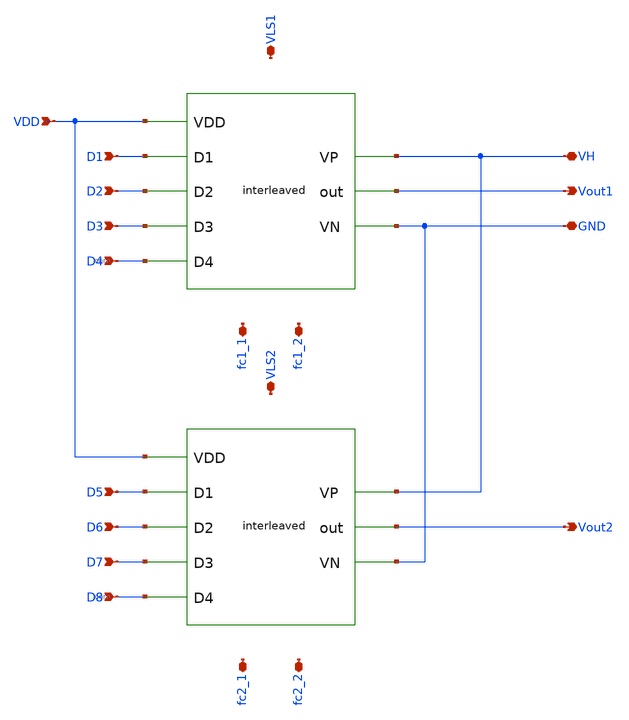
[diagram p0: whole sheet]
** sch_path: xschem/release/interleaved.sch
**.subckt interleaved D1 D2 D3 D4 D5 D6 D7 D8 VH GND Vout1 VDD Vout2 fc1_1 VLS1 VLS2 fc1_2 fc2_1
*+ fc2_2
*.ipin D1
*.ipin D2
*.ipin D3
*.ipin D4
*.ipin D5
*.ipin D6
*.ipin D7
*.ipin D8
*.iopin VH
*.iopin GND
*.opin Vout1
*.ipin VDD
*.opin Vout2
*.iopin fc1_1
*.iopin VLS1
*.iopin VLS2
*.iopin fc1_2
*.iopin fc2_1
*.iopin fc2_2
X1 VDD D6 D5 VH GND Vout2 D7 D8 core
X2 VDD D2 D1 VH GND Vout1 D3 D4 core
**.ends

* expanding   symbol:  core.sym # of pins=8
** sym_path: xschem/release/core.sym
** sch_path: xschem/release/core.sch
.subckt core VDD D2 D1 VP VN out D3 D4
*.opin out
*.iopin VP
*.ipin D1
*.ipin D2
*.ipin D3
*.ipin D4
*.iopin VDD
*.iopin VN
X1 net4 net3 net2 net1 out VP VN VN VN converter
x1 VP net5 net1 VDD level_shifter
x2 VP net6 net2 VDD level_shifter
x3 VP net7 net3 VDD level_shifter
x4 VP net8 net4 VDD level_shifter
.ends


* expanding   symbol:  converter.sym # of pins=9
** sym_path: xschem/hierarchy_sch/converter.sym
** sch_path: xschem/hierarchy_sch/converter.sch
.subckt converter s1 s2 s3 s4 out VP VN fc1_read fc2_read
*.ipin s1
*.ipin s2
*.ipin s3
*.ipin s4
*.iopin VP
*.iopin VN
*.opin fc1_read
*.opin fc2_read
*.iopin out
X1v s1 s2 s3 s4 fc1_read net1 out VP VN power_stage
CFLY fc1_read fc2_read 6.8n m=1
R1 fc2_read net1 0.001 m=1
.ends


* expanding   symbol:  level_shifter.sym # of pins=4
** sym_path: xschem/release/level_shifter.sym
** sch_path: xschem/release/level_shifter.sch
.subckt level_shifter VH vdd OUT IN
*.ipin IN
*.iopin vdd
*.iopin VH
*.opin OUT
XM11 net1 IN vdd vdd sky130_fd_pr__pfet_01v8 L=0.15 W=5 nf=1 ad='int((nf+1)/2) * W/nf * 0.29' as='int((nf+2)/2) * W/nf * 0.29'
+ pd='2*int((nf+1)/2) * (W/nf + 0.29)' ps='2*int((nf+2)/2) * (W/nf + 0.29)' nrd='0.29 / W' nrs='0.29 / W'
+ sa=0 sb=0 sd=0 mult=1 m=1
XM12 net1 IN GND GND sky130_fd_pr__nfet_01v8 L=0.15 W=5 nf=1 ad='int((nf+1)/2) * W/nf * 0.29' as='int((nf+2)/2) * W/nf * 0.29'
+ pd='2*int((nf+1)/2) * (W/nf + 0.29)' ps='2*int((nf+2)/2) * (W/nf + 0.29)' nrd='0.29 / W' nrs='0.29 / W'
+ sa=0 sb=0 sd=0 mult=1 m=1
XM15 net2 net3 VH VH sky130_fd_pr__pfet_g5v0d10v5 L=0.5 W=2 nf=1 ad='int((nf+1)/2) * W/nf * 0.29' as='int((nf+2)/2) * W/nf * 0.29'
+ pd='2*int((nf+1)/2) * (W/nf + 0.29)' ps='2*int((nf+2)/2) * (W/nf + 0.29)' nrd='0.29 / W' nrs='0.29 / W'
+ sa=0 sb=0 sd=0 mult=1 m=1
XM14 net3 net2 VH VH sky130_fd_pr__pfet_g5v0d10v5 L=0.5 W=2 nf=1 ad='int((nf+1)/2) * W/nf * 0.29' as='int((nf+2)/2) * W/nf * 0.29'
+ pd='2*int((nf+1)/2) * (W/nf + 0.29)' ps='2*int((nf+2)/2) * (W/nf + 0.29)' nrd='0.29 / W' nrs='0.29 / W'
+ sa=0 sb=0 sd=0 mult=1 m=1
XM16 net4 net2 VH VH sky130_fd_pr__pfet_g5v0d10v5 L=0.5 W=10 nf=1 ad='int((nf+1)/2) * W/nf * 0.29' as='int((nf+2)/2) * W/nf * 0.29'
+ pd='2*int((nf+1)/2) * (W/nf + 0.29)' ps='2*int((nf+2)/2) * (W/nf + 0.29)' nrd='0.29 / W' nrs='0.29 / W'
+ sa=0 sb=0 sd=0 mult=10 m=10
XM18 net2 net1 GND GND sky130_fd_pr__nfet_g5v0d10v5 L=0.5 W=12 nf=1 ad='int((nf+1)/2) * W/nf * 0.29'
+ as='int((nf+2)/2) * W/nf * 0.29' pd='2*int((nf+1)/2) * (W/nf + 0.29)' ps='2*int((nf+2)/2) * (W/nf + 0.29)'
+ nrd='0.29 / W' nrs='0.29 / W' sa=0 sb=0 sd=0 mult=1 m=1
XM13 net3 IN GND GND sky130_fd_pr__nfet_g5v0d10v5 L=0.5 W=12 nf=1 ad='int((nf+1)/2) * W/nf * 0.29' as='int((nf+2)/2) * W/nf * 0.29'
+ pd='2*int((nf+1)/2) * (W/nf + 0.29)' ps='2*int((nf+2)/2) * (W/nf + 0.29)' nrd='0.29 / W' nrs='0.29 / W'
+ sa=0 sb=0 sd=0 mult=1 m=1
XM17 net4 IN GND GND sky130_fd_pr__nfet_g5v0d10v5 L=0.5 W=10 nf=1 ad='int((nf+1)/2) * W/nf * 0.29' as='int((nf+2)/2) * W/nf * 0.29'
+ pd='2*int((nf+1)/2) * (W/nf + 0.29)' ps='2*int((nf+2)/2) * (W/nf + 0.29)' nrd='0.29 / W' nrs='0.29 / W'
+ sa=0 sb=0 sd=0 mult=10 m=10
XM7 OUT net4 VH VH sky130_fd_pr__pfet_g5v0d10v5 L=0.5 W=10 nf=1 ad='int((nf+1)/2) * W/nf * 0.29' as='int((nf+2)/2) * W/nf * 0.29'
+ pd='2*int((nf+1)/2) * (W/nf + 0.29)' ps='2*int((nf+2)/2) * (W/nf + 0.29)' nrd='0.29 / W' nrs='0.29 / W'
+ sa=0 sb=0 sd=0 mult={multip} m={multip}
XM10 OUT net4 GND GND sky130_fd_pr__nfet_g5v0d10v5 L=0.5 W=10 nf=1 ad='int((nf+1)/2) * W/nf * 0.29' as='int((nf+2)/2) * W/nf * 0.29'
+ pd='2*int((nf+1)/2) * (W/nf + 0.29)' ps='2*int((nf+2)/2) * (W/nf + 0.29)' nrd='0.29 / W' nrs='0.29 / W'
+ sa=0 sb=0 sd=0 mult={multip} m={multip}
**** begin user architecture code

*
* Parameters

*.PARAM BAT=1.8
.PARAM W12=12 W45=2 LLS=0.5 multip=40
*.option scale=1e-6
*.options TEMP = 65.0

* Models
*.lib /foss/pdk/sky130A/libs.tech/ngspice/sky130.lib.spice TT

*Fuentes******
*VBAT VDD 0 DC BAT
*VHIGH VH 0 DC 5
*vin IN 0 dc 0 PULSE (0 BAT .1n .1n .1n 10n 20n)

*COUT OUT 0 20p


*.options savecurrents
*.save all
*+ @M.XM12.msky130_fd_pr_nfet_01v8[id]

*.control
*tran 0.1n 100n
*plot v(IN) v(LS1) v(OUT) v(net6) i(@M.XM12.msky130_fd_pr_nfet_01v8[id])
*write LS_FINAL.raw
*.endc
*.end
*

**** end user architecture code
.ends


* expanding   symbol:  personal/3LFCC_AC3E/xschem/hierarchy_sch/power_stage.sym # of pins=9
** sym_path: xschem/hierarchy_sch/power_stage.sym
** sch_path: xschem/hierarchy_sch/power_stage.sch
.subckt power_stage s1 s2 s3 s4 fc1 fc2 out VP VN
*.ipin s1
*.ipin s2
*.ipin s3
*.ipin s4
*.iopin VP
*.iopin VN
*.opin out
*.opin fc1
*.opin fc2
X1 s2 fc1 s1 VP out transistor_group_one
X2 s4 fc2 s3 out VN transistor_group_two
.ends


* expanding   symbol:  personal/3LFCC_AC3E/xschem/hierarchy_sch/transistor_group_one.sym # of pins=5
** sym_path: xschem/hierarchy_sch/transistor_group_one.sym
** sch_path: xschem/hierarchy_sch/transistor_group_one.sch
.subckt transistor_group_one s2 fc1 s1 VP out
*.iopin VP
*.ipin s1
*.ipin s2
*.opin fc1
*.iopin out
XM3 out s2 fc1 fc1 sky130_fd_pr__pfet_g5v0d10v5 L=0.5 W=4.38 nf=1 ad='int((nf+1)/2) * W/nf * 0.29' as='int((nf+2)/2) * W/nf * 0.29'
+ pd='2*int((nf+1)/2) * (W/nf + 0.29)' ps='2*int((nf+2)/2) * (W/nf + 0.29)' nrd='0.29 / W' nrs='0.29 / W'
+ sa=0 sb=0 sd=0 mult=4506 m=4506
XM4 fc1 s1 VP VP sky130_fd_pr__pfet_g5v0d10v5 L=0.5 W=4.38 nf=1 ad='int((nf+1)/2) * W/nf * 0.29' as='int((nf+2)/2) * W/nf * 0.29'
+ pd='2*int((nf+1)/2) * (W/nf + 0.29)' ps='2*int((nf+2)/2) * (W/nf + 0.29)' nrd='0.29 / W' nrs='0.29 / W'
+ sa=0 sb=0 sd=0 mult=4506 m=4506
.ends


* expanding   symbol:  personal/3LFCC_AC3E/xschem/hierarchy_sch/transistor_group_two.sym # of pins=5
** sym_path: xschem/hierarchy_sch/transistor_group_two.sym
** sch_path: xschem/hierarchy_sch/transistor_group_two.sch
.subckt transistor_group_two s4 fc2 s3 out VN
*.iopin out
*.ipin s3
*.ipin s4
*.opin fc2
*.iopin VN
XM1 out s3 fc2 fc2 sky130_fd_pr__nfet_g5v0d10v5 L=0.5 W=4.38 nf=1 ad='int((nf+1)/2) * W/nf * 0.29' as='int((nf+2)/2) * W/nf * 0.29'
+ pd='2*int((nf+1)/2) * (W/nf + 0.29)' ps='2*int((nf+2)/2) * (W/nf + 0.29)' nrd='0.29 / W' nrs='0.29 / W'
+ sa=0 sb=0 sd=0 mult=2520 m=2520
XM2 fc2 s4 VN VN sky130_fd_pr__nfet_g5v0d10v5 L=0.5 W=4.38 nf=1 ad='int((nf+1)/2) * W/nf * 0.29' as='int((nf+2)/2) * W/nf * 0.29'
+ pd='2*int((nf+1)/2) * (W/nf + 0.29)' ps='2*int((nf+2)/2) * (W/nf + 0.29)' nrd='0.29 / W' nrs='0.29 / W'
+ sa=0 sb=0 sd=0 mult=2520 m=2520
.ends

.GLOBAL GND
.end
